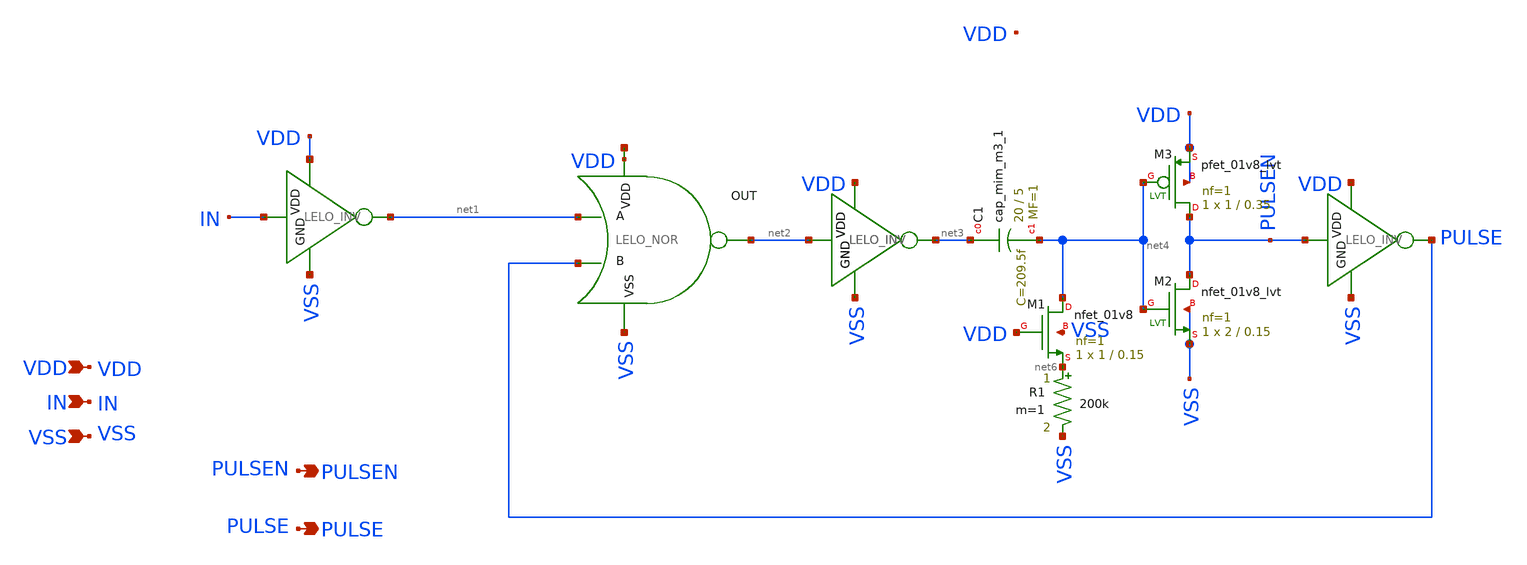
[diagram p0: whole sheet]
** sch_path: design/LELO_SVOD_SKY130A/LELO_ONESHOT.sch
**.subckt LELO_ONESHOT VDD IN VSS PULSEN PULSE
*.ipin VDD
*.ipin IN
*.ipin VSS
*.opin PULSEN
*.opin PULSE
x8 VDD PULSEN PULSE VSS LELO_INV
x12 net5 net2 net1 PULSE VSS LELO_NOR
x18 VDD IN net1 VSS LELO_INV
x1 VDD net2 net3 VSS LELO_INV
XM1 net4 VDD net6 VSS sky130_fd_pr__nfet_01v8 L=0.15 W=1 nf=1 ad='int((1 + 1)/2) * 1 / 1 * 0.29' as='int((1 + 2)/2) * 1 / 1 * 0.29'
+ pd='2*int((1 + 1)/2) * (1 / 1 + 0.29)' ps='2*int((1 + 2)/2) * (1 / 1 + 0.29)' nrd='0.29 / 1 ' nrs='0.29 / 1 '
+ sa=0 sb=0 sd=0 mult=1 m=1
x2 VDD net2 net3 VSS LELO_INV
R1 net6 VSS 200k m=1
XC1 net3 net4 sky130_fd_pr__cap_mim_m3_1 W=20 L=5 MF=1 m=1
XM2 PULSEN net4 VSS VSS sky130_fd_pr__nfet_01v8_lvt L=0.15 W=2 nf=1 ad='int((1 + 1)/2) * 2 / 1 * 0.29'
+ as='int((1 + 2)/2) * 2 / 1 * 0.29' pd='2*int((1 + 1)/2) * (2 / 1 + 0.29)' ps='2*int((1 + 2)/2) * (2 / 1 + 0.29)'
+ nrd='0.29 / 2 ' nrs='0.29 / 2 ' sa=0 sb=0 sd=0 mult=1 m=1
XM3 PULSEN net4 VDD VDD sky130_fd_pr__pfet_01v8_lvt L=0.35 W=1 nf=1 ad='int((1 + 1)/2) * 1 / 1 * 0.29'
+ as='int((1 + 2)/2) * 1 / 1 * 0.29' pd='2*int((1 + 1)/2) * (1 / 1 + 0.29)' ps='2*int((1 + 2)/2) * (1 / 1 + 0.29)'
+ nrd='0.29 / 1 ' nrs='0.29 / 1 ' sa=0 sb=0 sd=0 mult=1 m=1
**.ends

* expanding   symbol:  LELO_SVOD_SKY130A/LELO_INV.sym # of pins=4
** sym_path: design/LELO_SVOD_SKY130A/LELO_INV.sym
** sch_path: design/LELO_SVOD_SKY130A/LELO_INV.sch
.subckt LELO_INV VDD VIN VOUT GND
*.ipin VIN
*.ipin VDD
*.ipin GND
*.opin VOUT
XM1 VOUT VIN GND GND sky130_fd_pr__nfet_01v8_lvt L=0.15 W=1 nf=1 ad='int((1 + 1)/2) * 1 / 1 * 0.29' as='int((1 + 2)/2) * 1 / 1 * 0.29'
+ pd='2*int((1 + 1)/2) * (1 / 1 + 0.29)' ps='2*int((1 + 2)/2) * (1 / 1 + 0.29)' nrd='0.29 / 1 ' nrs='0.29 / 1 '
+ sa=0 sb=0 sd=0 mult=1 m=1
XM2 VOUT VIN VDD VDD sky130_fd_pr__pfet_01v8_lvt L=0.35 W=1 nf=1 ad='int((1 + 1)/2) * 1 / 1 * 0.29' as='int((1 + 2)/2) * 1 / 1 * 0.29'
+ pd='2*int((1 + 1)/2) * (1 / 1 + 0.29)' ps='2*int((1 + 2)/2) * (1 / 1 + 0.29)' nrd='0.29 / 1 ' nrs='0.29 / 1 '
+ sa=0 sb=0 sd=0 mult=2 m=2
.ends


* expanding   symbol:  LELO_SVOD_SKY130A/LELO_NOR.sym # of pins=5
** sym_path: design/LELO_SVOD_SKY130A/LELO_NOR.sym
** sch_path: design/LELO_SVOD_SKY130A/LELO_NOR.sch
.subckt LELO_NOR VDD OUT A B VSS
*.ipin VDD
*.ipin VSS
*.opin OUT
*.ipin A
*.ipin B
XM2 OUT B VSS VSS sky130_fd_pr__nfet_01v8 L=0.15 W=2 nf=1 ad='int((1 + 1)/2) * 2 / 1 * 0.29' as='int((1 + 2)/2) * 2 / 1 * 0.29'
+ pd='2*int((1 + 1)/2) * (2 / 1 + 0.29)' ps='2*int((1 + 2)/2) * (2 / 1 + 0.29)' nrd='0.29 / 2 ' nrs='0.29 / 2 '
+ sa=0 sb=0 sd=0 mult=1 m=1
XM1 OUT A VSS VSS sky130_fd_pr__nfet_01v8 L=0.15 W=2 nf=1 ad='int((1 + 1)/2) * 2 / 1 * 0.29' as='int((1 + 2)/2) * 2 / 1 * 0.29'
+ pd='2*int((1 + 1)/2) * (2 / 1 + 0.29)' ps='2*int((1 + 2)/2) * (2 / 1 + 0.29)' nrd='0.29 / 2 ' nrs='0.29 / 2 '
+ sa=0 sb=0 sd=0 mult=1 m=1
XM3 OUT B net1 VDD sky130_fd_pr__pfet_01v8 L=0.15 W=4 nf=1 ad='int((1 + 1)/2) * 4 / 1 * 0.29' as='int((1 + 2)/2) * 4 / 1 * 0.29'
+ pd='2*int((1 + 1)/2) * (4 / 1 + 0.29)' ps='2*int((1 + 2)/2) * (4 / 1 + 0.29)' nrd='0.29 / 4 ' nrs='0.29 / 4 '
+ sa=0 sb=0 sd=0 mult=1 m=1
XM4 net1 A VDD VDD sky130_fd_pr__pfet_01v8 L=0.15 W=4 nf=1 ad='int((1 + 1)/2) * 4 / 1 * 0.29' as='int((1 + 2)/2) * 4 / 1 * 0.29'
+ pd='2*int((1 + 1)/2) * (4 / 1 + 0.29)' ps='2*int((1 + 2)/2) * (4 / 1 + 0.29)' nrd='0.29 / 4 ' nrs='0.29 / 4 '
+ sa=0 sb=0 sd=0 mult=1 m=1
.ends

.end
